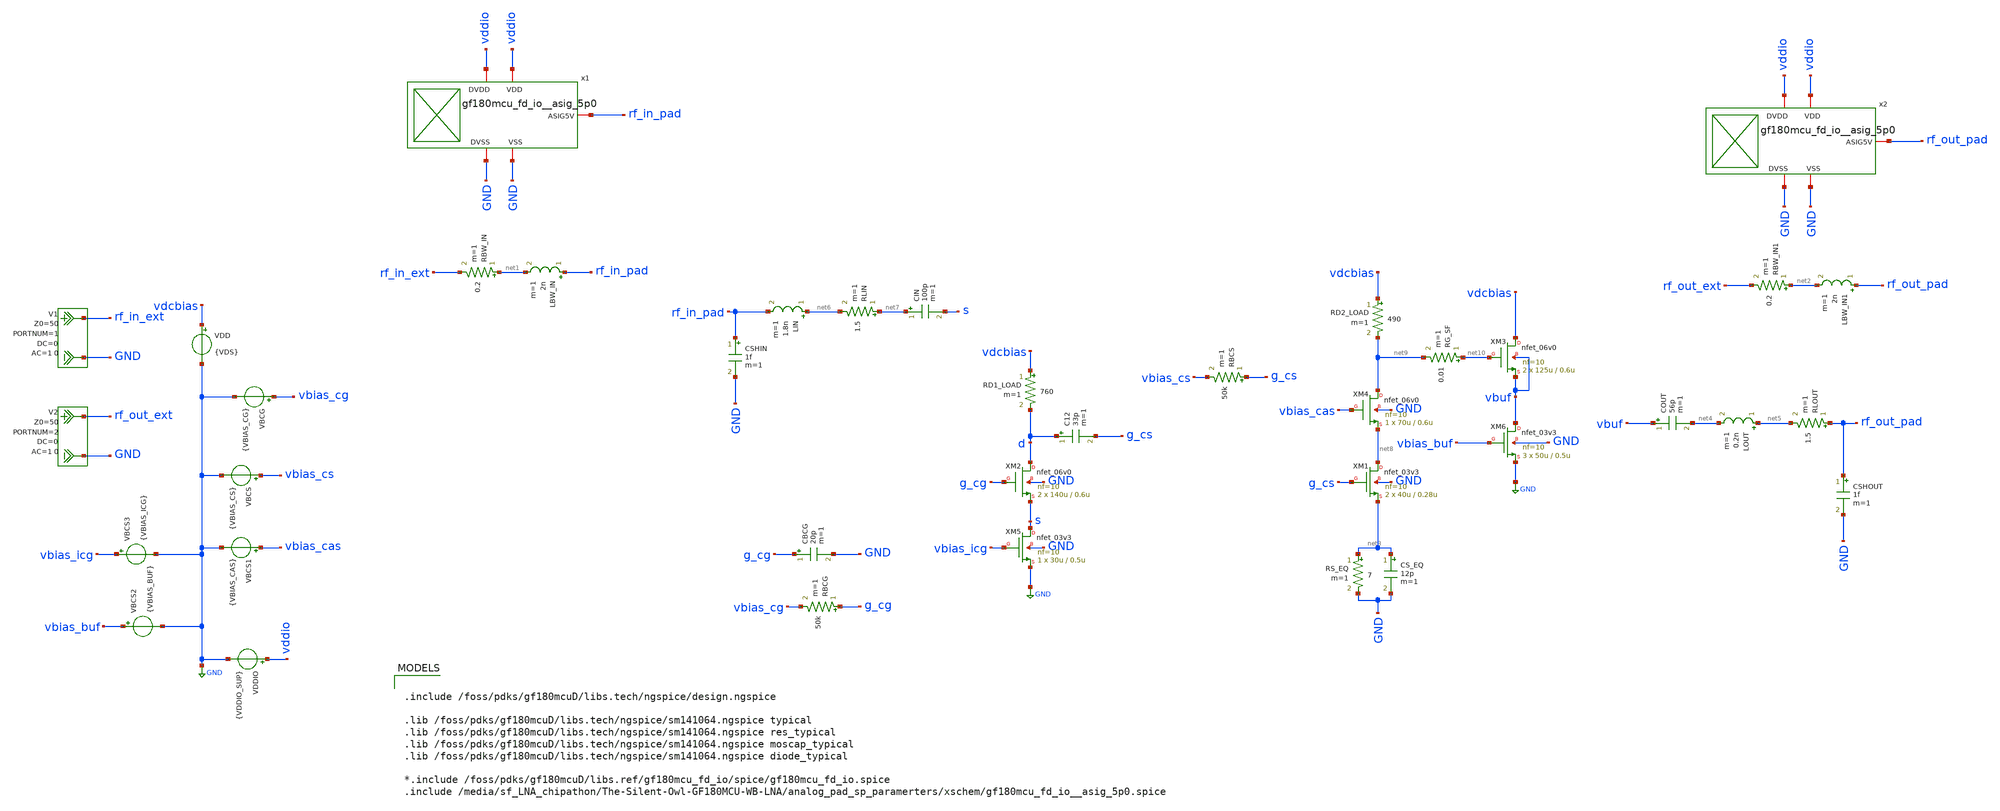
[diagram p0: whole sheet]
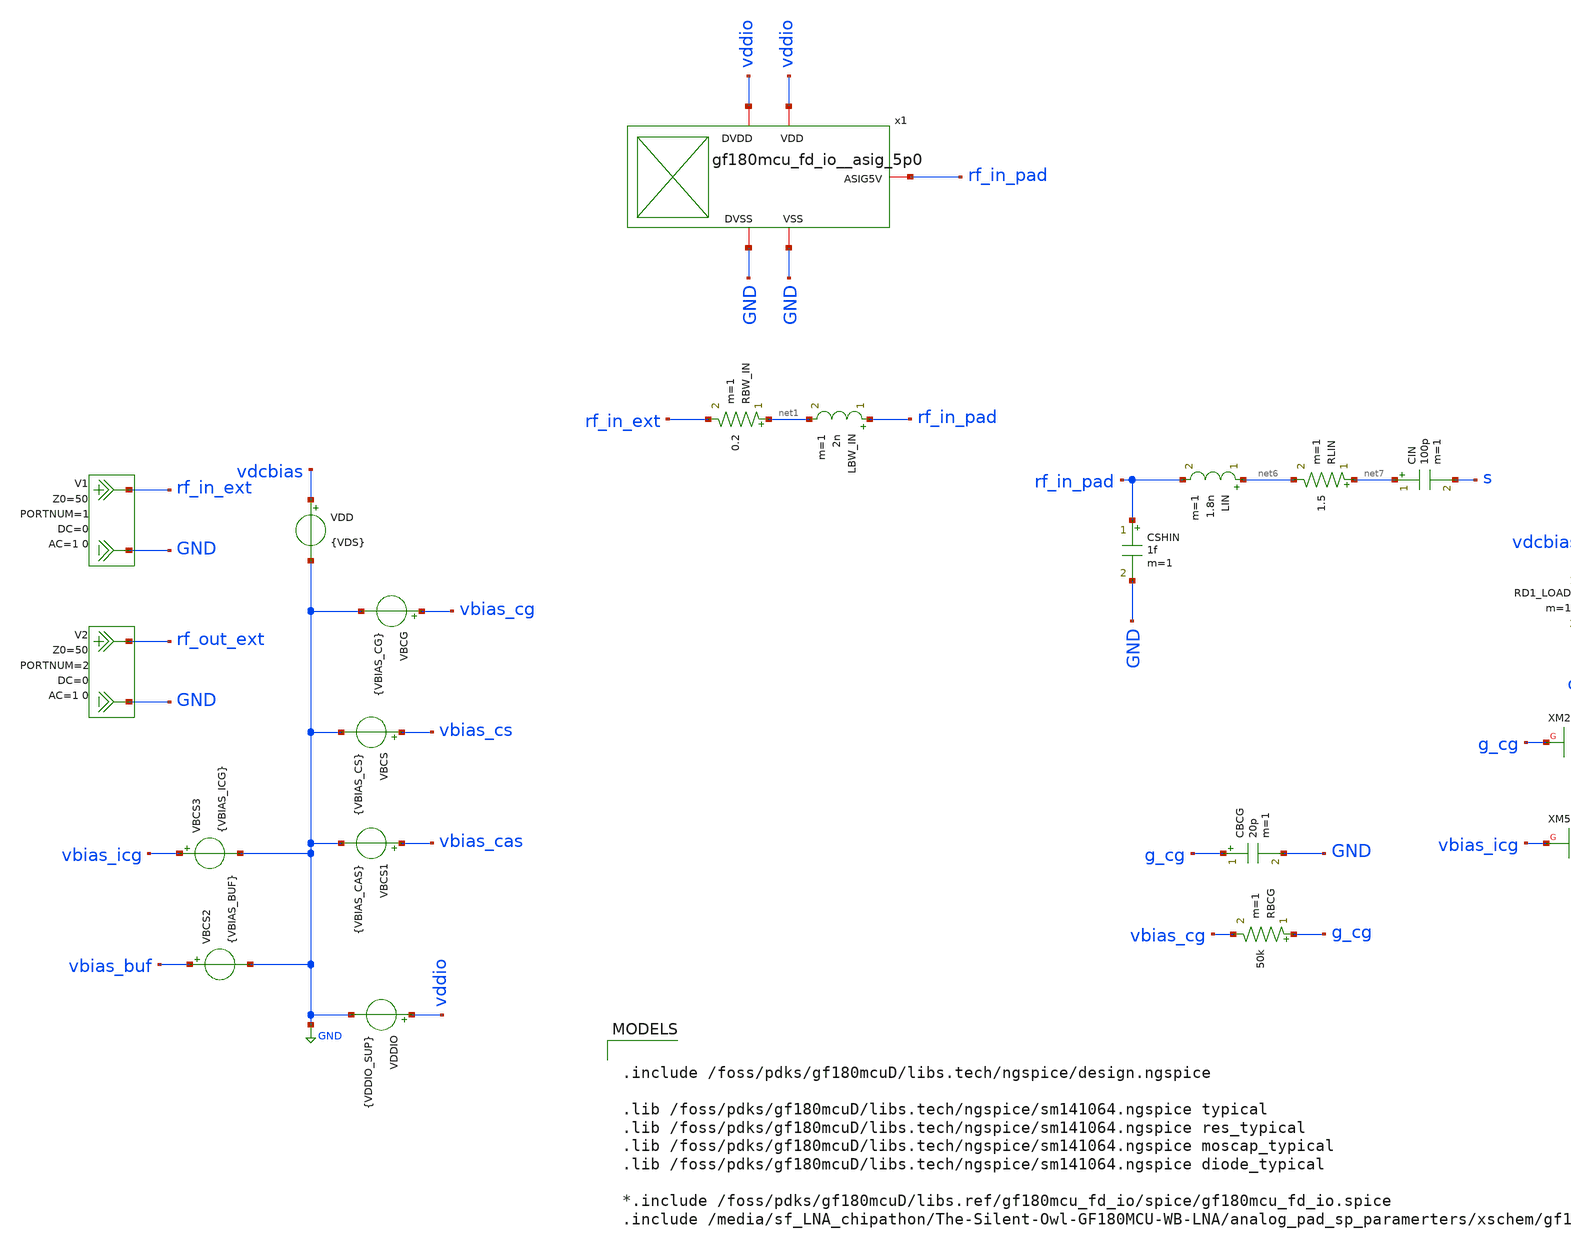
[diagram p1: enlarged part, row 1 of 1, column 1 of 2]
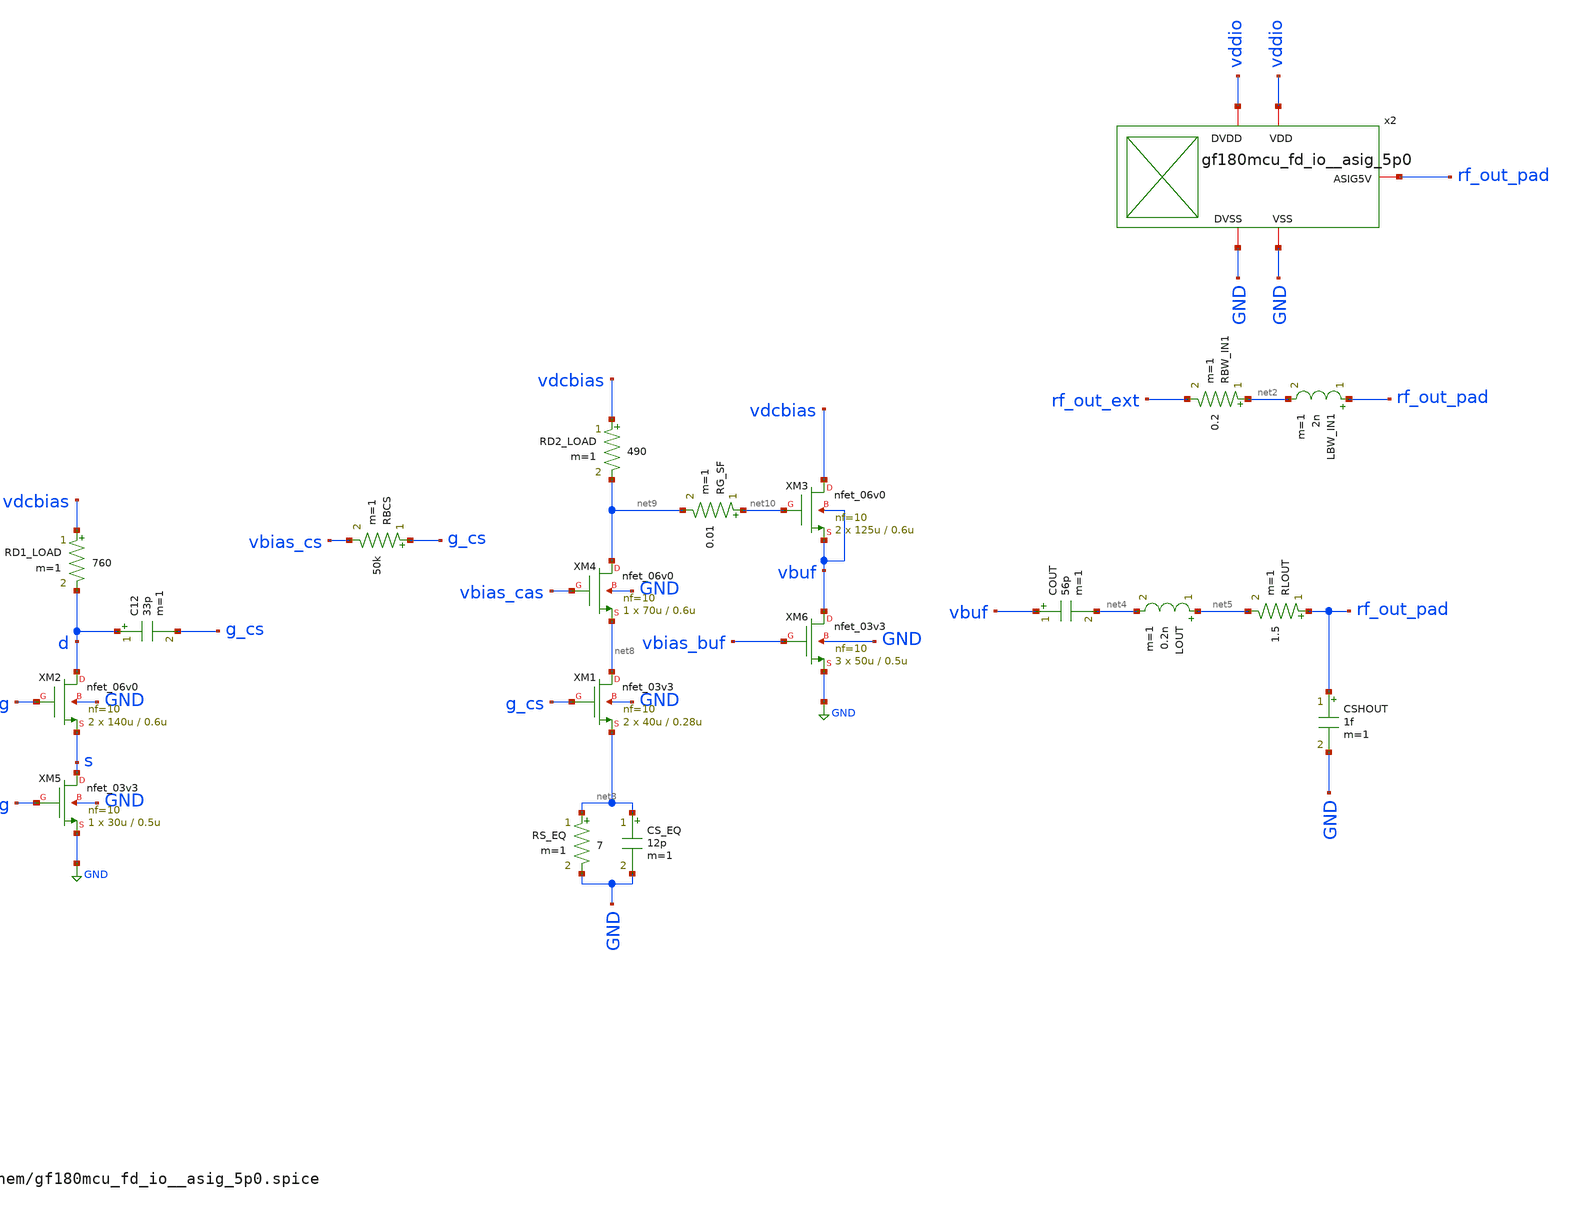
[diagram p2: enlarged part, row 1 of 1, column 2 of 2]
** sch_path: NFmin_Simulation/simulations/lna_core_06V_cgcs.sch
**.subckt lna_core_06V_cgcs
VBCG vbias_cg GND {VBIAS_CG}
VDD vdcbias GND {VDS}
C12 d g_cs 33p m=1
CIN net7 s 100p m=1
V1 rf_in_ext GND DC 0 AC 1 0 portnum 1 z0 50
V2 rf_out_ext GND DC 0 AC 1 0 portnum 2 z0 50
XM2 d g_cg s GND nfet_06v0 L=0.6u W=140u nf=10 ad='int((nf+1)/2) * W/nf * 0.18u' as='int((nf+2)/2) * W/nf * 0.18u'
+ pd='2*int((nf+1)/2) * (W/nf + 0.18u)' ps='2*int((nf+2)/2) * (W/nf + 0.18u)' nrd='0.18u / W' nrs='0.18u / W'
+ sa=0 sb=0 sd=0 m=2
RBCG g_cg vbias_cg 50k m=1
CBCG g_cg GND 20p m=1
x1 rf_in_pad vddio GND vddio GND gf180mcu_fd_io__asig_5p0
LBW_IN rf_in_pad net1 2n m=1
RBW_IN net1 rf_in_ext 0.2 m=1
VDDIO vddio GND {VDDIO_SUP}
x2 rf_out_pad vddio GND vddio GND gf180mcu_fd_io__asig_5p0
LBW_IN1 rf_out_pad net2 2n m=1
RBW_IN1 net2 rf_out_ext 0.2 m=1
VBCS vbias_cs GND {VBIAS_CS}
RD1_LOAD vdcbias d 760 m=1
RBCS g_cs vbias_cs 50k m=1
RD2_LOAD vdcbias net9 490 m=1
XM3 vdcbias net10 vbuf vbuf nfet_06v0 L=0.6u W=125u nf=10 ad='int((nf+1)/2) * W/nf * 0.18u' as='int((nf+2)/2) * W/nf * 0.18u'
+ pd='2*int((nf+1)/2) * (W/nf + 0.18u)' ps='2*int((nf+2)/2) * (W/nf + 0.18u)' nrd='0.18u / W' nrs='0.18u / W'
+ sa=0 sb=0 sd=0 m=2
COUT vbuf net4 56p m=1
LOUT net5 net4 0.2n m=1
RLOUT rf_out_pad net5 1.5 m=1
CSHOUT rf_out_pad GND 1f m=1
CSHIN rf_in_pad GND 1f m=1
LIN net6 rf_in_pad 1.8n m=1
RLIN net7 net6 1.5 m=1
XM4 net9 vbias_cas net8 GND nfet_06v0 L=0.6u W=70u nf=10 ad='int((nf+1)/2) * W/nf * 0.18u' as='int((nf+2)/2) * W/nf * 0.18u'
+ pd='2*int((nf+1)/2) * (W/nf + 0.18u)' ps='2*int((nf+2)/2) * (W/nf + 0.18u)' nrd='0.18u / W' nrs='0.18u / W'
+ sa=0 sb=0 sd=0 m=1
VBCS1 vbias_cas GND {VBIAS_CAS}
VBCS2 vbias_buf GND {VBIAS_BUF}
VBCS3 vbias_icg GND {VBIAS_ICG}
XM5 s vbias_icg GND GND nfet_03v3 L=0.5u W=30u nf=10 ad='int((nf+1)/2) * W/nf * 0.18u' as='int((nf+2)/2) * W/nf * 0.18u'
+ pd='2*int((nf+1)/2) * (W/nf + 0.18u)' ps='2*int((nf+2)/2) * (W/nf + 0.18u)' nrd='0.18u / W' nrs='0.18u / W'
+ sa=0 sb=0 sd=0 m=1
XM6 vbuf vbias_buf GND GND nfet_03v3 L=0.5u W=50u nf=10 ad='int((nf+1)/2) * W/nf * 0.18u' as='int((nf+2)/2) * W/nf * 0.18u'
+ pd='2*int((nf+1)/2) * (W/nf + 0.18u)' ps='2*int((nf+2)/2) * (W/nf + 0.18u)' nrd='0.18u / W' nrs='0.18u / W'
+ sa=0 sb=0 sd=0 m=3
RS_EQ net3 GND 7 m=1
CS_EQ net3 GND 12p m=1
XM1 net8 g_cs net3 GND nfet_03v3 L=0.28u W=40u nf=10 ad='int((nf+1)/2) * W/nf * 0.18u' as='int((nf+2)/2) * W/nf * 0.18u'
+ pd='2*int((nf+1)/2) * (W/nf + 0.18u)' ps='2*int((nf+2)/2) * (W/nf + 0.18u)' nrd='0.18u / W' nrs='0.18u / W'
+ sa=0 sb=0 sd=0 m=2
RG_SF net10 net9 0.01 m=1
**** begin user architecture code

.include /foss/pdks/gf180mcuD/libs.tech/ngspice/design.ngspice

.lib /foss/pdks/gf180mcuD/libs.tech/ngspice/sm141064.ngspice typical
.lib /foss/pdks/gf180mcuD/libs.tech/ngspice/sm141064.ngspice res_typical
.lib /foss/pdks/gf180mcuD/libs.tech/ngspice/sm141064.ngspice moscap_typical
.lib /foss/pdks/gf180mcuD/libs.tech/ngspice/sm141064.ngspice diode_typical

*.include /foss/pdks/gf180mcuD/libs.ref/gf180mcu_fd_io/spice/gf180mcu_fd_io.spice
.include /media/sf_LNA_chipathon/The-Silent-Owl-GF180MCU-WB-LNA/analog_pad_sp_paramerters/xschem/gf180mcu_fd_io__asig_5p0.spice



* =============================================================================
* FIXED SUPPLY / PACKAGE VALUES
* =============================================================================
.param VDS=5.0
.param VDDIO_SUP=5.0
.param L_BW=2n
.param R_BW=0.2

* =============================================================================
* FIXED INPUT NETWORK
* =============================================================================
.param L_IN=1.80n
.param R_L_IN=1.5
.param CIN_VAL=100p
.param C_SH_IN=1f

* =============================================================================
* FIXED XM2 COMMON-GATE INPUT STAGE
* =============================================================================
.param VBIAS_CG=2.00
.param W_CG=140u
.param M_CG=2
.param L_CG=0.60u
.param RD1=760
.param RBIAS_CG=50k
.param CBYP_CG=20p

* =============================================================================
* FIXED MIXED-VOLTAGE XM1/XM4 STAGE
* =============================================================================
.param C12_VAL=33p

.param VBIAS_CS=0.95
.param W_CS=40u
.param M_CS=2
.param L_CS=0.28u
.param RBIAS_CS=50k

.param VBIAS_CAS=3.30
.param W_CAS=70u
.param M_CAS=1
.param L_CAS=0.60u
.param RD2=490

* XM1 source equalizer
.param RS_EQ=7
.param CSEQ_VAL=12p

* =============================================================================
* FIXED BODY-TIED SOURCE FOLLOWER
* =============================================================================
.param W_SF=125u
.param M_SF=2
.param L_SF=0.60u
.param RG_SF_VAL=0.01

* =============================================================================
* FIXED OUTPUT NETWORK
* =============================================================================
.param COUT_VAL=56p
.param L_OUT=0.20n
.param R_L_OUT=1.5
.param C_SH_OUT=1f

* =============================================================================
* FIXED XM5 COMMON-GATE CURRENT SINK
* =============================================================================
.param VBIAS_ICG=1.55
.param L_BIAS_CG=0.50u
.param W_BIAS_CG=30u
.param M_BIAS_CG=1

* =============================================================================
* FIXED XM6 SOURCE-FOLLOWER CURRENT SINK
* =============================================================================
.param VBIAS_BUF=2.40
.param L_BIAS_SF=0.50u
.param W_BIAS_SF=50u
.param M_BIAS_SF=3

* Disabled series-RC high-frequency snubber
.param C_STAB_VAL=1f
.param R_STAB_VAL=50
C_STAB net9 n_stab {C_STAB_VAL}
R_STAB n_stab GND {R_STAB_VAL}

.control
set noaskquit
set wr_singlescale
set wr_vecnames
set numdgt=10
set filetype=ascii
set plotwinsize=0

* =============================================================================
* SPECIFICATION LIMITS
* =============================================================================

* Original 2.30–2.50 GHz design-band limits
let TB_S11_LIMIT=-10
let TB_S22_LIMIT=-10
let TB_S21_LIMIT=15
let TB_NF_LIMIT=3.5
let TB_RIPPLE_LIMIT=1.2
let TB_PDC_LIMIT=300
let TB_MU_LIMIT=1.05
let TB_DELTA_LIMIT=1.0

* New exact 1–6 GHz broadband limits
let BB_S11_LIMIT=-10
let BB_S22_LIMIT=-10
let BB_S21_LIMIT=10
let BB_NF_LIMIT=5

* DC and reliability checks
let MIN_SATMARGIN_SINK=0.20
let MIN_SATMARGIN_XM1=0.25
let MIN_SATMARGIN_CORE=0.40
let MIN_SATMARGIN_CG=0.50
let MAX_03V3_TERMINAL=3.00

* Append frequency tables after the report headers.
set appendwrite

* =============================================================================
* INITIALIZE THE TWO REPORT FILES
* =============================================================================

echo ============================================================ > lna_v28_detailed_report.txt
echo LNA_V28_FIXED_DUAL_BAND_DETAILED_REPORT >> lna_v28_detailed_report.txt
echo NO_PARAMETER_SWEEPS >> lna_v28_detailed_report.txt
echo EXACT_BANDS 2.30_TO_2.50_GHZ AND 1_TO_6_GHZ >> lna_v28_detailed_report.txt
echo ============================================================ >> lna_v28_detailed_report.txt
echo FIXED_PARAMETERS >> lna_v28_detailed_report.txt
echo SUPPLY VDS 5.0 VDDIO 5.0 >> lna_v28_detailed_report.txt
echo INPUT LIN 1.80n RLIN 1.5 CIN 100p CSHIN 1f >> lna_v28_detailed_report.txt
echo XM2 WCG 140u MCG 2 LCG 0.60u VBCG 2.00 RD1 760 >> lna_v28_detailed_report.txt
echo XM1 WCS 40u MCS 2 LCS 0.28u VBCS 0.95 >> lna_v28_detailed_report.txt
echo XM4 WCAS 70u MCAS 1 LCAS 0.60u VBCAS 3.30 RD2 490 >> lna_v28_detailed_report.txt
echo INTERSTAGE C12 33p REQ 7 CEQ 12p >> lna_v28_detailed_report.txt
echo FOLLOWER WSF 125u MSF 2 LSF 0.60u RG 0.01 >> lna_v28_detailed_report.txt
echo OUTPUT COUT 56p LOUT 0.20n RLOUT 1.5 CSHOUT 1f >> lna_v28_detailed_report.txt
echo XM5 W5 30u M5 1 L5 0.50u VBICG 1.55 >> lna_v28_detailed_report.txt
echo XM6 W6 50u M6 3 L6 0.50u VBUF_BIAS 2.40 >> lna_v28_detailed_report.txt
echo SNUBBER CSTAB 1f RSTAB 50 DISABLED_EFFECTIVELY >> lna_v28_detailed_report.txt
echo ============================================================ >> lna_v28_detailed_report.txt

echo ============================================================ > lna_v28_summary_report.txt
echo LNA_V28_FIXED_DUAL_BAND_SUMMARY_REPORT >> lna_v28_summary_report.txt
echo NO_PARAMETER_SWEEPS >> lna_v28_summary_report.txt
echo ============================================================ >> lna_v28_summary_report.txt
echo BAND_1 2.30_TO_2.50_GHZ >> lna_v28_summary_report.txt
echo BAND_1_LIMITS S11_LT_-10 S22_LT_-10 S21_GT_15 NF_LT_3P5 RIPPLE_LT_1P2 PDC_LT_300 MU_GT_1P05
+ DELTA_LT_1 >> lna_v28_summary_report.txt
echo BAND_2 1_TO_6_GHZ >> lna_v28_summary_report.txt
echo BAND_2_LIMITS S11_LT_-10 S22_LT_-10 S21_GT_10 NF_LT_5 >> lna_v28_summary_report.txt
echo ============================================================ >> lna_v28_summary_report.txt

* =============================================================================
* 1. DC OPERATING POINT AND DEVICE HEADROOM
* =============================================================================
op

let PDCmW=1e3*(abs(i(VDD))*v(vdcbias)+abs(i(VDDIO))*v(vddio))
let IDD=abs(i(VDD))
let IIO=abs(i(VDDIO))

let Vsrc1=v(net3)
let VX1=v(net8)
let V9=v(net9)
let VbufDC=v(vbuf)

let ID1=abs(@m.xm1.m0[id])
let GM1=@m.xm1.m0[gm]
let GDS1=@m.xm1.m0[gds]
let VGS1=v(g_cs)-v(net3)
let VGD1=v(g_cs)-v(net8)
let VGB1=v(g_cs)
let VDS1=v(net8)-v(net3)
let VDSAT1=abs(@m.xm1.m0[vdsat])
let SAT1=VDS1-VDSAT1
let GMID1=GM1/ID1

let ID2=abs(@m.xm2.m0[id])
let GM2=@m.xm2.m0[gm]
let GMB2=@m.xm2.m0[gmbs]
let GDS2=@m.xm2.m0[gds]
let VDS2=v(d)-v(s)
let VDSAT2=abs(@m.xm2.m0[vdsat])
let SAT2=VDS2-VDSAT2
let GMID2=GM2/ID2

let ID3=abs(@m.xm3.m0[id])
let GM3=@m.xm3.m0[gm]
let GDS3=@m.xm3.m0[gds]
let VDS3=v(vdcbias)-v(vbuf)
let VDSAT3=abs(@m.xm3.m0[vdsat])
let SAT3=VDS3-VDSAT3
let GMID3=GM3/ID3

let ID4=abs(@m.xm4.m0[id])
let GM4=@m.xm4.m0[gm]
let GDS4=@m.xm4.m0[gds]
let VDS4=v(net9)-v(net8)
let VDSAT4=abs(@m.xm4.m0[vdsat])
let SAT4=VDS4-VDSAT4
let GMID4=GM4/ID4

let ID5=abs(@m.xm5.m0[id])
let GM5=@m.xm5.m0[gm]
let GDS5=@m.xm5.m0[gds]
let VDS5=v(s)
let VDSAT5=abs(@m.xm5.m0[vdsat])
let SAT5=VDS5-VDSAT5
let GMID5=GM5/ID5
let RO5=1/GDS5

let ID6=abs(@m.xm6.m0[id])
let GM6=@m.xm6.m0[gm]
let GDS6=@m.xm6.m0[gds]
let VDS6=v(vbuf)
let VDSAT6=abs(@m.xm6.m0[vdsat])
let SAT6=VDS6-VDSAT6
let GMID6=GM6/ID6
let RO6=1/GDS6

let GMRatio25=(GM2+GMB2)/GM5

let DCPass=1
if SAT1 < MIN_SATMARGIN_XM1
  let DCPass=0
end
if SAT2 < MIN_SATMARGIN_CG
  let DCPass=0
end
if SAT3 < MIN_SATMARGIN_CORE
  let DCPass=0
end
if SAT4 < MIN_SATMARGIN_CORE
  let DCPass=0
end
if SAT5 < MIN_SATMARGIN_SINK
  let DCPass=0
end
if SAT6 < MIN_SATMARGIN_SINK
  let DCPass=0
end
if abs(VGS1) > MAX_03V3_TERMINAL
  let DCPass=0
end
if abs(VGD1) > MAX_03V3_TERMINAL
  let DCPass=0
end
if abs(VGB1) > MAX_03V3_TERMINAL
  let DCPass=0
end
if abs(VDS1) > MAX_03V3_TERMINAL
  let DCPass=0
end

* Preserve DC scalars after the OP plot is destroyed.
set OP_PDC=$&PDCmW
set OP_IDD=$&IDD
set OP_IIO=$&IIO
set OP_VSRC1=$&Vsrc1
set OP_VX1=$&VX1
set OP_V9=$&V9
set OP_VBUF=$&VbufDC

set OP_ID1=$&ID1
set OP_GM1=$&GM1
set OP_GDS1=$&GDS1
set OP_GMID1=$&GMID1
set OP_VGS1=$&VGS1
set OP_VGD1=$&VGD1
set OP_VGB1=$&VGB1
set OP_VDS1=$&VDS1
set OP_SAT1=$&SAT1

set OP_ID2=$&ID2
set OP_GM2=$&GM2
set OP_GMB2=$&GMB2
set OP_GDS2=$&GDS2
set OP_GMID2=$&GMID2
set OP_VDS2=$&VDS2
set OP_SAT2=$&SAT2

set OP_ID3=$&ID3
set OP_GM3=$&GM3
set OP_GDS3=$&GDS3
set OP_GMID3=$&GMID3
set OP_VDS3=$&VDS3
set OP_SAT3=$&SAT3

set OP_ID4=$&ID4
set OP_GM4=$&GM4
set OP_GDS4=$&GDS4
set OP_GMID4=$&GMID4
set OP_VDS4=$&VDS4
set OP_SAT4=$&SAT4

set OP_ID5=$&ID5
set OP_GM5=$&GM5
set OP_GDS5=$&GDS5
set OP_GMID5=$&GMID5
set OP_RO5=$&RO5
set OP_VDS5=$&VDS5
set OP_SAT5=$&SAT5

set OP_ID6=$&ID6
set OP_GM6=$&GM6
set OP_GDS6=$&GDS6
set OP_GMID6=$&GMID6
set OP_RO6=$&RO6
set OP_VDS6=$&VDS6
set OP_SAT6=$&SAT6

set OP_RATIO25=$&GMRatio25
set OP_DCPASS=$&DCPass

echo DC_OPERATING_POINT >> lna_v28_detailed_report.txt
echo POWER PDC_MW $OP_PDC IDD_A $OP_IDD IIO_A $OP_IIO >> lna_v28_detailed_report.txt
echo NODES NET3_XM1_SOURCE $OP_VSRC1 NET8_XM1_DRAIN $OP_VX1 NET9_XM4_DRAIN $OP_V9 VBUF $OP_VBUF >>
+ lna_v28_detailed_report.txt
echo XM1 ID $OP_ID1 GM $OP_GM1 GDS $OP_GDS1 GMID $OP_GMID1 VGS $OP_VGS1 VGD $OP_VGD1 VGB $OP_VGB1
+ VDS $OP_VDS1 SAT_MARGIN $OP_SAT1 >> lna_v28_detailed_report.txt
echo XM2 ID $OP_ID2 GM $OP_GM2 GMB $OP_GMB2 GDS $OP_GDS2 GMID $OP_GMID2 VDS $OP_VDS2 SAT_MARGIN
+ $OP_SAT2 >> lna_v28_detailed_report.txt
echo XM3 ID $OP_ID3 GM $OP_GM3 GDS $OP_GDS3 GMID $OP_GMID3 VDS $OP_VDS3 SAT_MARGIN $OP_SAT3 >>
+ lna_v28_detailed_report.txt
echo XM4 ID $OP_ID4 GM $OP_GM4 GDS $OP_GDS4 GMID $OP_GMID4 VDS $OP_VDS4 SAT_MARGIN $OP_SAT4 >>
+ lna_v28_detailed_report.txt
echo XM5 ID $OP_ID5 GM $OP_GM5 GDS $OP_GDS5 GMID $OP_GMID5 RO $OP_RO5 VDS $OP_VDS5 SAT_MARGIN
+ $OP_SAT5 >> lna_v28_detailed_report.txt
echo XM6 ID $OP_ID6 GM $OP_GM6 GDS $OP_GDS6 GMID $OP_GMID6 RO $OP_RO6 VDS $OP_VDS6 SAT_MARGIN
+ $OP_SAT6 >> lna_v28_detailed_report.txt
echo GM_RATIO_XM2EFF_OVER_XM5 $OP_RATIO25 >> lna_v28_detailed_report.txt
echo DC_PASS $OP_DCPASS >> lna_v28_detailed_report.txt
echo ============================================================ >> lna_v28_detailed_report.txt

destroy $curplot

* =============================================================================
* 2. EXACT 2.30 TO 2.50 GHz ANALYSIS
* =============================================================================
sp lin 401 2.30G 2.50G 1

let FGHz=frequency/1e9
let S11db=db(s_1_1)
let S21db=db(s_2_1)
let S12db=db(s_1_2)
let S22db=db(s_2_2)
let NFdb=real(NF)
let NFMINdb=real(NFmin)

let Delta=s_1_1*s_2_2-s_1_2*s_2_1
let DeltaMag=mag(Delta)
let A11=mag(s_1_1)
let A12=mag(s_1_2)
let A21=mag(s_2_1)
let A22=mag(s_2_2)

let Mu=(1-A11*A11)/(mag(s_2_2-Delta*conj(s_1_1))+mag(s_1_2*s_2_1))
let Mup=(1-A22*A22)/(mag(s_1_1-Delta*conj(s_2_2))+mag(s_1_2*s_2_1))
let Kfactor=(1-A11*A11-A22*A22+DeltaMag*DeltaMag)/(2*A12*A21)

let Zin=50*(1+s_1_1)/(1-s_1_1)
let Zout=50*(1+s_2_2)/(1-s_2_2)
let ZinRe=real(Zin)
let ZinIm=imag(Zin)
let ZoutRe=real(Zout)
let ZoutIm=imag(Zout)
let VSWRin=(1+A11)/(1-A11)
let VSWRout=(1+A22)/(1-A22)

let S11Worst=maximum(S11db)
let S21Min=minimum(S21db)
let S21Max=maximum(S21db)
let S21Ripple=S21Max-S21Min
let S21Tilt=abs(S21db[0]-S21db[400])
let S12Worst=maximum(S12db)
let S22Worst=maximum(S22db)
let NFWorst=maximum(NFdb)
let NFMINWorst=maximum(NFMINdb)
let MuMin=minimum(Mu)
let MupMin=minimum(Mup)
let KMin=minimum(Kfactor)
let DeltaMax=maximum(DeltaMag)
let VSWRinMax=maximum(VSWRin)
let VSWRoutMax=maximum(VSWRout)

* Exact 2.4 GHz values: index 200 of the 401-point linear sweep.
let S11At2p4=S11db[200]
let S21At2p4=S21db[200]
let S12At2p4=S12db[200]
let S22At2p4=S22db[200]
let NFAt2p4=NFdb[200]
let NFMINAt2p4=NFMINdb[200]
let MuAt2p4=Mu[200]
let MupAt2p4=Mup[200]
let KAt2p4=Kfactor[200]
let DeltaAt2p4=DeltaMag[200]
let ZinReAt2p4=ZinRe[200]
let ZinImAt2p4=ZinIm[200]
let ZoutReAt2p4=ZoutRe[200]
let ZoutImAt2p4=ZoutIm[200]

let TBPassCount=0
if S11Worst < TB_S11_LIMIT
  let TBPassCount=TBPassCount+1
end
if S22Worst < TB_S22_LIMIT
  let TBPassCount=TBPassCount+1
end
if S21Min > TB_S21_LIMIT
  let TBPassCount=TBPassCount+1
end
if NFWorst < TB_NF_LIMIT
  let TBPassCount=TBPassCount+1
end
if S21Ripple < TB_RIPPLE_LIMIT
  let TBPassCount=TBPassCount+1
end
if $OP_PDC < TB_PDC_LIMIT
  let TBPassCount=TBPassCount+1
end
if MuMin > TB_MU_LIMIT
  let TBPassCount=TBPassCount+1
end
if MupMin > TB_MU_LIMIT
  let TBPassCount=TBPassCount+1
end
if DeltaMax < TB_DELTA_LIMIT
  let TBPassCount=TBPassCount+1
end

let TBPass=0
if TBPassCount = 9
  let TBPass=1
end

set TB_S11W=$&S11Worst
set TB_S21MIN=$&S21Min
set TB_S21MAX=$&S21Max
set TB_RIPPLE=$&S21Ripple
set TB_TILT=$&S21Tilt
set TB_S12W=$&S12Worst
set TB_S22W=$&S22Worst
set TB_NFW=$&NFWorst
set TB_NFMINW=$&NFMINWorst
set TB_MUMIN=$&MuMin
set TB_MUPMIN=$&MupMin
set TB_KMIN=$&KMin
set TB_DELTAMAX=$&DeltaMax
set TB_VSWRINMAX=$&VSWRinMax
set TB_VSWROUTMAX=$&VSWRoutMax
set TB_PASSCOUNT=$&TBPassCount
set TB_PASS=$&TBPass

set TB_S11_2P4=$&S11At2p4
set TB_S21_2P4=$&S21At2p4
set TB_S12_2P4=$&S12At2p4
set TB_S22_2P4=$&S22At2p4
set TB_NF_2P4=$&NFAt2p4
set TB_NFMIN_2P4=$&NFMINAt2p4
set TB_MU_2P4=$&MuAt2p4
set TB_MUP_2P4=$&MupAt2p4
set TB_K_2P4=$&KAt2p4
set TB_DELTA_2P4=$&DeltaAt2p4
set TB_ZINRE_2P4=$&ZinReAt2p4
set TB_ZINIM_2P4=$&ZinImAt2p4
set TB_ZOUTRE_2P4=$&ZoutReAt2p4
set TB_ZOUTIM_2P4=$&ZoutImAt2p4

echo BAND_1_FULL_FREQUENCY_DATA_2P30_TO_2P50_GHZ >> lna_v28_detailed_report.txt
echo COLUMNS FGHz S11db S21db S12db S22db NFdb NFMINdb Mu Mup Kfactor DeltaMag ZinRe ZinIm ZoutRe
+ ZoutIm VSWRin VSWRout >> lna_v28_detailed_report.txt
wrdata lna_v28_detailed_report.txt
  FGHz S11db S21db S12db S22db NFdb NFMINdb
  Mu Mup Kfactor DeltaMag ZinRe ZinIm ZoutRe ZoutIm VSWRin VSWRout
echo END_BAND_1_FULL_FREQUENCY_DATA >> lna_v28_detailed_report.txt
echo ============================================================ >> lna_v28_detailed_report.txt

destroy $curplot

* =============================================================================
* 3. EXACT 1 TO 6 GHz ANALYSIS
* =============================================================================
sp lin 2001 1G 6G 1

let FGHz=frequency/1e9
let S11db=db(s_1_1)
let S21db=db(s_2_1)
let S12db=db(s_1_2)
let S22db=db(s_2_2)
let NFdb=real(NF)
let NFMINdb=real(NFmin)

let Delta=s_1_1*s_2_2-s_1_2*s_2_1
let DeltaMag=mag(Delta)
let A11=mag(s_1_1)
let A12=mag(s_1_2)
let A21=mag(s_2_1)
let A22=mag(s_2_2)

let Mu=(1-A11*A11)/(mag(s_2_2-Delta*conj(s_1_1))+mag(s_1_2*s_2_1))
let Mup=(1-A22*A22)/(mag(s_1_1-Delta*conj(s_2_2))+mag(s_1_2*s_2_1))
let Kfactor=(1-A11*A11-A22*A22+DeltaMag*DeltaMag)/(2*A12*A21)

let Zin=50*(1+s_1_1)/(1-s_1_1)
let Zout=50*(1+s_2_2)/(1-s_2_2)
let ZinRe=real(Zin)
let ZinIm=imag(Zin)
let ZoutRe=real(Zout)
let ZoutIm=imag(Zout)
let VSWRin=(1+A11)/(1-A11)
let VSWRout=(1+A22)/(1-A22)

let S11Worst=maximum(S11db)
let S21Min=minimum(S21db)
let S21Max=maximum(S21db)
let S21Ripple=S21Max-S21Min
let S21Tilt=abs(S21db[0]-S21db[2000])
let S12Worst=maximum(S12db)
let S22Worst=maximum(S22db)
let NFWorst=maximum(NFdb)
let NFMINWorst=maximum(NFMINdb)
let MuMin=minimum(Mu)
let MupMin=minimum(Mup)
let KMin=minimum(Kfactor)
let DeltaMax=maximum(DeltaMag)
let VSWRinMax=maximum(VSWRin)
let VSWRoutMax=maximum(VSWRout)

let BBPassCount=0
if S11Worst < BB_S11_LIMIT
  let BBPassCount=BBPassCount+1
end
if S22Worst < BB_S22_LIMIT
  let BBPassCount=BBPassCount+1
end
if S21Min > BB_S21_LIMIT
  let BBPassCount=BBPassCount+1
end
if NFWorst < BB_NF_LIMIT
  let BBPassCount=BBPassCount+1
end

let BBPass=0
if BBPassCount = 4
  let BBPass=1
end

set BB_S11W=$&S11Worst
set BB_S21MIN=$&S21Min
set BB_S21MAX=$&S21Max
set BB_RIPPLE=$&S21Ripple
set BB_TILT=$&S21Tilt
set BB_S12W=$&S12Worst
set BB_S22W=$&S22Worst
set BB_NFW=$&NFWorst
set BB_NFMINW=$&NFMINWorst
set BB_MUMIN=$&MuMin
set BB_MUPMIN=$&MupMin
set BB_KMIN=$&KMin
set BB_DELTAMAX=$&DeltaMax
set BB_VSWRINMAX=$&VSWRinMax
set BB_VSWROUTMAX=$&VSWRoutMax
set BB_PASSCOUNT=$&BBPassCount
set BB_PASS=$&BBPass

echo BAND_2_FULL_FREQUENCY_DATA_1_TO_6_GHZ >> lna_v28_detailed_report.txt
echo COLUMNS FGHz S11db S21db S12db S22db NFdb NFMINdb Mu Mup Kfactor DeltaMag ZinRe ZinIm ZoutRe
+ ZoutIm VSWRin VSWRout >> lna_v28_detailed_report.txt
wrdata lna_v28_detailed_report.txt
  FGHz S11db S21db S12db S22db NFdb NFMINdb
  Mu Mup Kfactor DeltaMag ZinRe ZinIm ZoutRe ZoutIm VSWRin VSWRout
echo END_BAND_2_FULL_FREQUENCY_DATA >> lna_v28_detailed_report.txt
echo ============================================================ >> lna_v28_detailed_report.txt

destroy $curplot

* =============================================================================
* 4. INTERACTIVE PLOTS: DISPLAY 0 TO 7 GHz
* =============================================================================
* The actual RF analysis begins at 1 MHz because SP/noise analysis is not
* evaluated at exactly DC. All graph x-axes are displayed from 0 to 7 GHz.
sp lin 2801 1MEG 7G 1

let FGHz=frequency/1e9
let S11db=db(s_1_1)
let S21db=db(s_2_1)
let S12db=db(s_1_2)
let S22db=db(s_2_2)
let NFdb=real(NF)
let NFMINdb=real(NFmin)

let Delta=s_1_1*s_2_2-s_1_2*s_2_1
let DeltaMag=mag(Delta)
let A11=mag(s_1_1)
let A12=mag(s_1_2)
let A21=mag(s_2_1)
let A22=mag(s_2_2)

let Mu=(1-A11*A11)/(mag(s_2_2-Delta*conj(s_1_1))+mag(s_1_2*s_2_1))
let Mup=(1-A22*A22)/(mag(s_1_1-Delta*conj(s_2_2))+mag(s_1_2*s_2_1))
let Kfactor=(1-A11*A11-A22*A22+DeltaMag*DeltaMag)/(2*A12*A21)

let Zin=50*(1+s_1_1)/(1-s_1_1)
let Zout=50*(1+s_2_2)/(1-s_2_2)
let ZinRe=real(Zin)
let ZinIm=imag(Zin)
let ZoutRe=real(Zout)
let ZoutIm=imag(Zout)
let VSWRin=(1+A11)/(1-A11)
let VSWRout=(1+A22)/(1-A22)

setscale FGHz

* NF and NFmin together
plot NFdb NFMINdb xlimit 0 7

* Combined response plots retained from the previous deck
plot S21db NFdb xlimit 0 7
plot S11db S22db xlimit 0 7

* Each S-parameter on a separate graph
plot S11db xlimit 0 7
plot S21db xlimit 0 7
plot S12db xlimit 0 7
plot S22db xlimit 0 7

* All S-parameters on one graph
plot S11db S21db S12db S22db xlimit 0 7

* Stability
plot Mu Mup xlimit 0 7
plot Kfactor xlimit 0 7
plot DeltaMag xlimit 0 7

* Impedance and VSWR
plot ZinRe ZinIm xlimit 0 7
plot ZoutRe ZoutIm xlimit 0 7
plot VSWRin VSWRout xlimit 0 7

* Do not destroy this plot. Keep all graph windows interactive.

* =============================================================================
* 5. WIDEBAND STABILITY CHECK: 10 MHz TO 30 GHz
* =============================================================================
sp dec 100 10Meg 30Gig 1

let WBFrequencyGHz=frequency/1e9
let WBDelta=s_1_1*s_2_2-s_1_2*s_2_1
let WBDeltaMag=mag(WBDelta)
let WBA11=mag(s_1_1)
let WBA12=mag(s_1_2)
let WBA21=mag(s_2_1)
let WBA22=mag(s_2_2)

let WBMu=(1-WBA11*WBA11)/(mag(s_2_2-WBDelta*conj(s_1_1))+mag(s_1_2*s_2_1))
let WBMup=(1-WBA22*WBA22)/(mag(s_1_1-WBDelta*conj(s_2_2))+mag(s_1_2*s_2_1))
let WBK=(1-WBA11*WBA11-WBA22*WBA22+WBDeltaMag*WBDeltaMag)/(2*WBA12*WBA21)

let WBMuMin=minimum(WBMu)
let WBMupMin=minimum(WBMup)
let WBKMin=minimum(WBK)
let WBDeltaMax=maximum(WBDeltaMag)

set WB_MUMIN=$&WBMuMin
set WB_MUPMIN=$&WBMupMin
set WB_KMIN=$&WBKMin
set WB_DELTAMAX=$&WBDeltaMax

* =============================================================================
* FINAL AGGREGATE SECTIONS IN THE DETAILED REPORT
* =============================================================================

echo BAND_1_AGGREGATE_RESULTS_2P30_TO_2P50_GHZ >> lna_v28_detailed_report.txt
echo S11_WORST_DB $TB_S11W >> lna_v28_detailed_report.txt
echo S21_MIN_DB $TB_S21MIN S21_MAX_DB $TB_S21MAX RIPPLE_DB $TB_RIPPLE TILT_DB $TB_TILT >>
+ lna_v28_detailed_report.txt
echo S12_WORST_DB $TB_S12W S22_WORST_DB $TB_S22W >> lna_v28_detailed_report.txt
echo NF_WORST_DB $TB_NFW NFMIN_WORST_DB $TB_NFMINW >> lna_v28_detailed_report.txt
echo STABILITY MU_MIN $TB_MUMIN MUP_MIN $TB_MUPMIN K_MIN $TB_KMIN DELTA_MAX $TB_DELTAMAX >>
+ lna_v28_detailed_report.txt
echo VSWR INPUT_MAX $TB_VSWRINMAX OUTPUT_MAX $TB_VSWROUTMAX >> lna_v28_detailed_report.txt
echo AT_2P4GHZ S11_DB $TB_S11_2P4 S21_DB $TB_S21_2P4 S12_DB $TB_S12_2P4 S22_DB $TB_S22_2P4 NF_DB
+ $TB_NF_2P4 NFMIN_DB $TB_NFMIN_2P4 >> lna_v28_detailed_report.txt
echo AT_2P4GHZ MU $TB_MU_2P4 MUP $TB_MUP_2P4 K $TB_K_2P4 DELTA $TB_DELTA_2P4 >>
+ lna_v28_detailed_report.txt
echo AT_2P4GHZ ZIN_RE $TB_ZINRE_2P4 ZIN_IM $TB_ZINIM_2P4 ZOUT_RE $TB_ZOUTRE_2P4 ZOUT_IM
+ $TB_ZOUTIM_2P4 >> lna_v28_detailed_report.txt
echo BAND_1_RESULT PASSCOUNT $TB_PASSCOUNT OF_9 PASS $TB_PASS >> lna_v28_detailed_report.txt
echo ============================================================ >> lna_v28_detailed_report.txt

echo BAND_2_AGGREGATE_RESULTS_1_TO_6_GHZ >> lna_v28_detailed_report.txt
echo S11_WORST_DB $BB_S11W >> lna_v28_detailed_report.txt
echo S21_MIN_DB $BB_S21MIN S21_MAX_DB $BB_S21MAX RIPPLE_DB $BB_RIPPLE TILT_DB $BB_TILT >>
+ lna_v28_detailed_report.txt
echo S12_WORST_DB $BB_S12W S22_WORST_DB $BB_S22W >> lna_v28_detailed_report.txt
echo NF_WORST_DB $BB_NFW NFMIN_WORST_DB $BB_NFMINW >> lna_v28_detailed_report.txt
echo STABILITY MU_MIN $BB_MUMIN MUP_MIN $BB_MUPMIN K_MIN $BB_KMIN DELTA_MAX $BB_DELTAMAX >>
+ lna_v28_detailed_report.txt
echo VSWR INPUT_MAX $BB_VSWRINMAX OUTPUT_MAX $BB_VSWROUTMAX >> lna_v28_detailed_report.txt
echo BAND_2_RESULT PASSCOUNT $BB_PASSCOUNT OF_4 PASS $BB_PASS >> lna_v28_detailed_report.txt
echo ============================================================ >> lna_v28_detailed_report.txt

echo WIDEBAND_STABILITY_10MHZ_TO_30GHZ >> lna_v28_detailed_report.txt
echo MU_MIN $WB_MUMIN MUP_MIN $WB_MUPMIN K_MIN $WB_KMIN DELTA_MAX $WB_DELTAMAX >>
+ lna_v28_detailed_report.txt
echo ============================================================ >> lna_v28_detailed_report.txt

* =============================================================================
* CONCISE SUMMARY REPORT
* =============================================================================

echo FIXED_POINT >> lna_v28_summary_report.txt
echo WCG_140u VBCG_2P00 RD1_760 W5_30u VBICG_1P55 C12_33p REQ_7 CEQ_12p RD2_490 COUT_56p >>
+ lna_v28_summary_report.txt
echo POWER PDC_MW $OP_PDC IDD_A $OP_IDD DC_PASS $OP_DCPASS >> lna_v28_summary_report.txt
echo ============================================================ >> lna_v28_summary_report.txt

echo BAND_1_RESULTS_2P30_TO_2P50_GHZ >> lna_v28_summary_report.txt
echo S11_WORST_DB $TB_S11W LIMIT_LT_-10 >> lna_v28_summary_report.txt
echo S22_WORST_DB $TB_S22W LIMIT_LT_-10 >> lna_v28_summary_report.txt
echo S21_MIN_DB $TB_S21MIN LIMIT_GT_15 >> lna_v28_summary_report.txt
echo S21_MAX_DB $TB_S21MAX RIPPLE_DB $TB_RIPPLE LIMIT_LT_1P2 >> lna_v28_summary_report.txt
echo NF_WORST_DB $TB_NFW LIMIT_LT_3P5 >> lna_v28_summary_report.txt
echo MU_MIN $TB_MUMIN MUP_MIN $TB_MUPMIN DELTA_MAX $TB_DELTAMAX >> lna_v28_summary_report.txt
echo PASSCOUNT $TB_PASSCOUNT OF_9 BAND_1_PASS $TB_PASS >> lna_v28_summary_report.txt
echo ============================================================ >> lna_v28_summary_report.txt

echo BAND_2_RESULTS_1_TO_6_GHZ >> lna_v28_summary_report.txt
echo S11_WORST_DB $BB_S11W LIMIT_LT_-10 >> lna_v28_summary_report.txt
echo S22_WORST_DB $BB_S22W LIMIT_LT_-10 >> lna_v28_summary_report.txt
echo S21_MIN_DB $BB_S21MIN LIMIT_GT_10 >> lna_v28_summary_report.txt
echo S21_MAX_DB $BB_S21MAX RIPPLE_DB $BB_RIPPLE >> lna_v28_summary_report.txt
echo NF_WORST_DB $BB_NFW LIMIT_LT_5 >> lna_v28_summary_report.txt
echo MU_MIN $BB_MUMIN MUP_MIN $BB_MUPMIN DELTA_MAX $BB_DELTAMAX >> lna_v28_summary_report.txt
echo PASSCOUNT $BB_PASSCOUNT OF_4 BAND_2_PASS $BB_PASS >> lna_v28_summary_report.txt
echo ============================================================ >> lna_v28_summary_report.txt

echo WIDEBAND_STABILITY_10MHZ_TO_30GHZ >> lna_v28_summary_report.txt
echo MU_MIN $WB_MUMIN MUP_MIN $WB_MUPMIN K_MIN $WB_KMIN DELTA_MAX $WB_DELTAMAX >>
+ lna_v28_summary_report.txt
echo ============================================================ >> lna_v28_summary_report.txt

echo LNA_V28_SIMULATION_COMPLETE
echo DETAILED_REPORT lna_v28_detailed_report.txt
echo SUMMARY_REPORT lna_v28_summary_report.txt
echo INTERACTIVE_PLOTS_OPENED 14
echo NGSPICE_LEFT_OPEN_FOR_CURSOR_ZOOM_AND_TRACE_INSPECTION

.endc


**** end user architecture code
**.ends
.GLOBAL GND
.end
